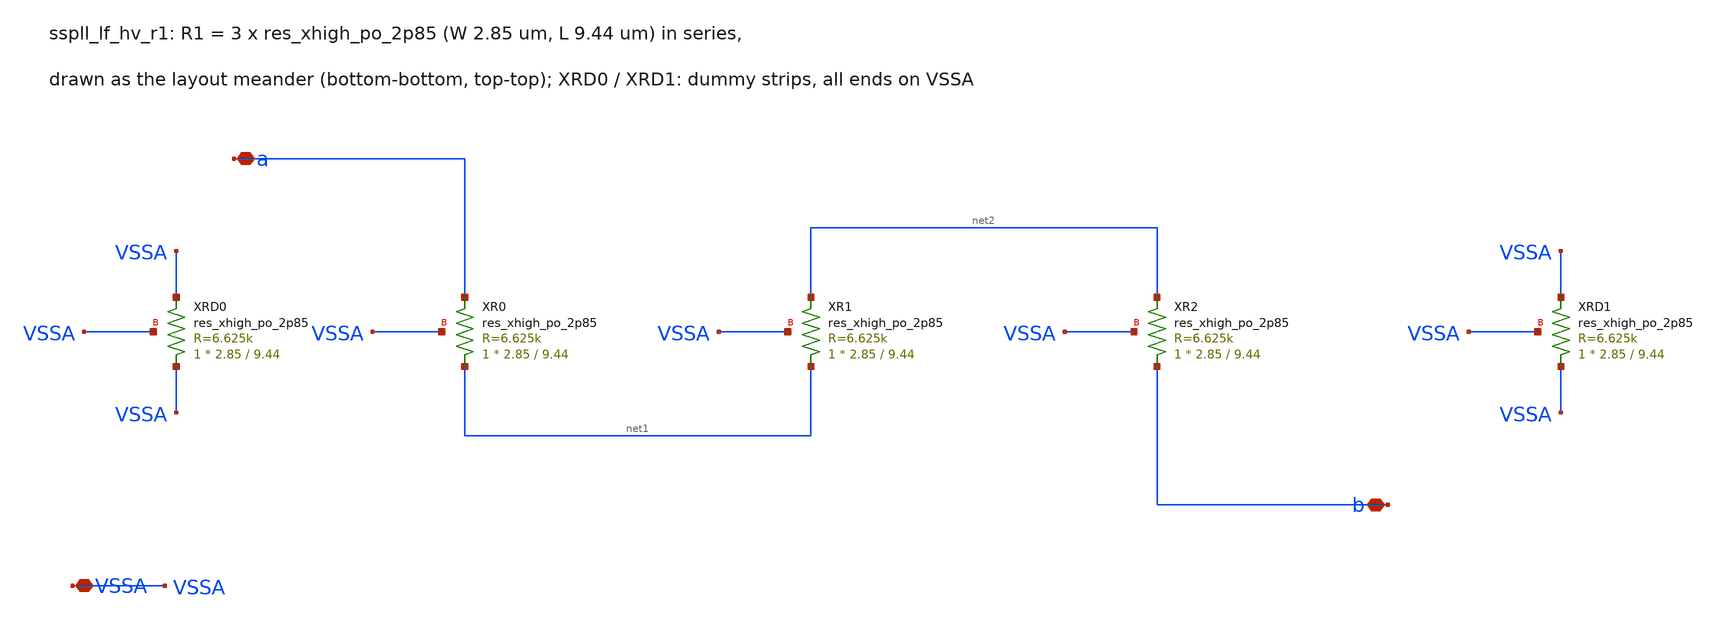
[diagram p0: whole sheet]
** sch_path: xschem/lf_hv/sspll_lf_hv_r1.sch
**.subckt sspll_lf_hv_r1 a b VSSA
*.iopin a
*.iopin b
*.iopin VSSA
XXR0 net1 a VSSA sky130_fd_pr__res_xhigh_po_2p85 L=9.44 mult=1 m=1
XXR1 net1 net2 VSSA sky130_fd_pr__res_xhigh_po_2p85 L=9.44 mult=1 m=1
XXR2 b net2 VSSA sky130_fd_pr__res_xhigh_po_2p85 L=9.44 mult=1 m=1
XXRD0 VSSA VSSA VSSA sky130_fd_pr__res_xhigh_po_2p85 L=9.44 mult=1 m=1
XXRD1 VSSA VSSA VSSA sky130_fd_pr__res_xhigh_po_2p85 L=9.44 mult=1 m=1
**.ends
.end
